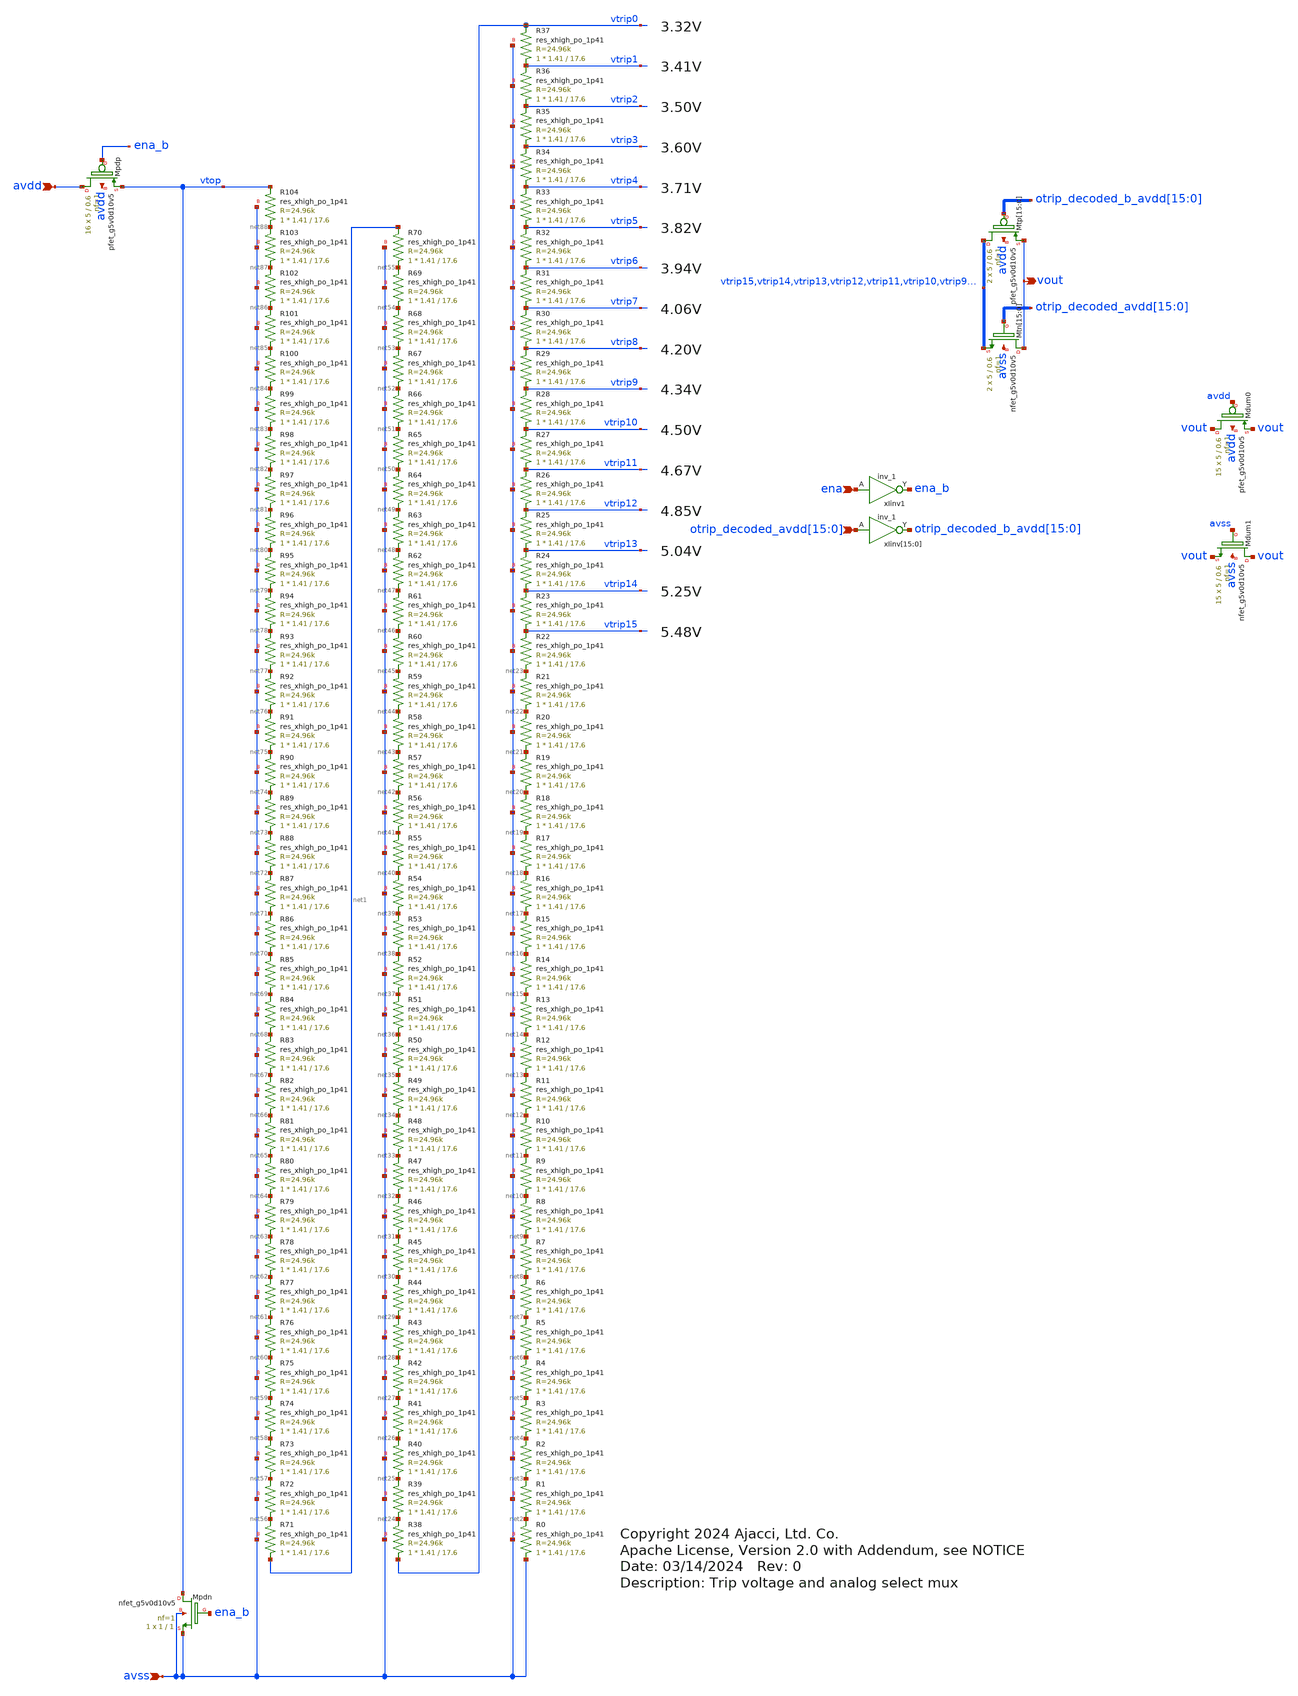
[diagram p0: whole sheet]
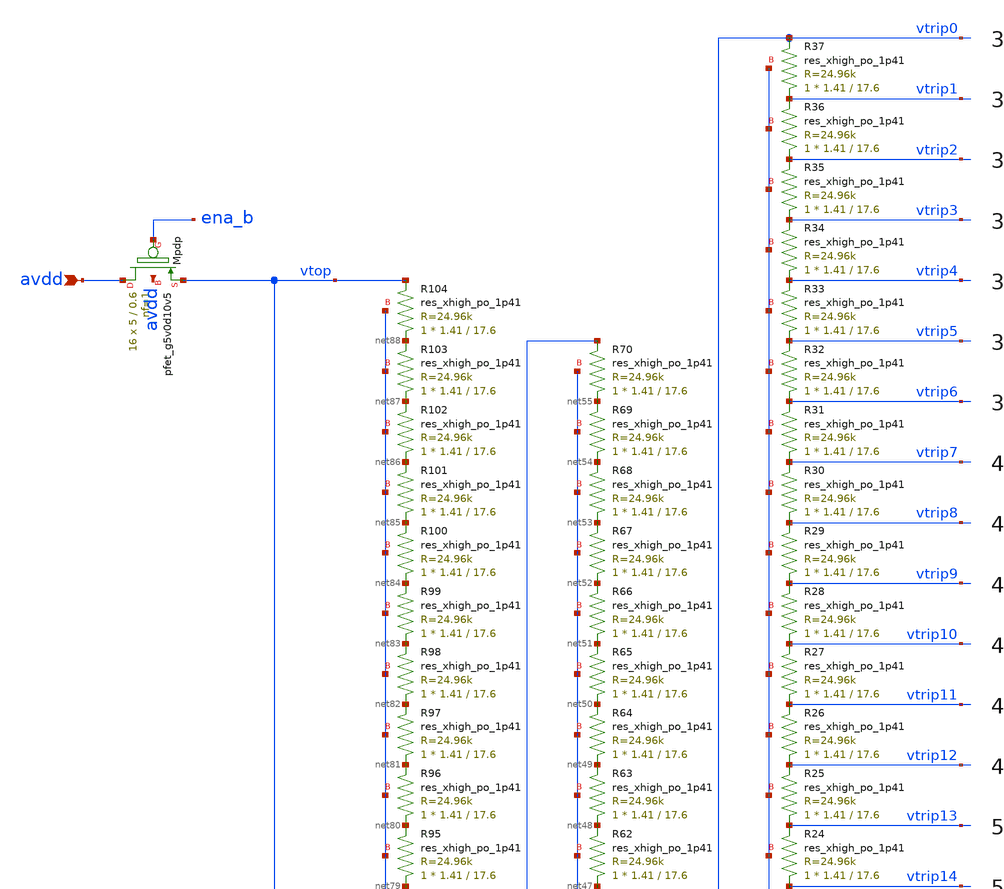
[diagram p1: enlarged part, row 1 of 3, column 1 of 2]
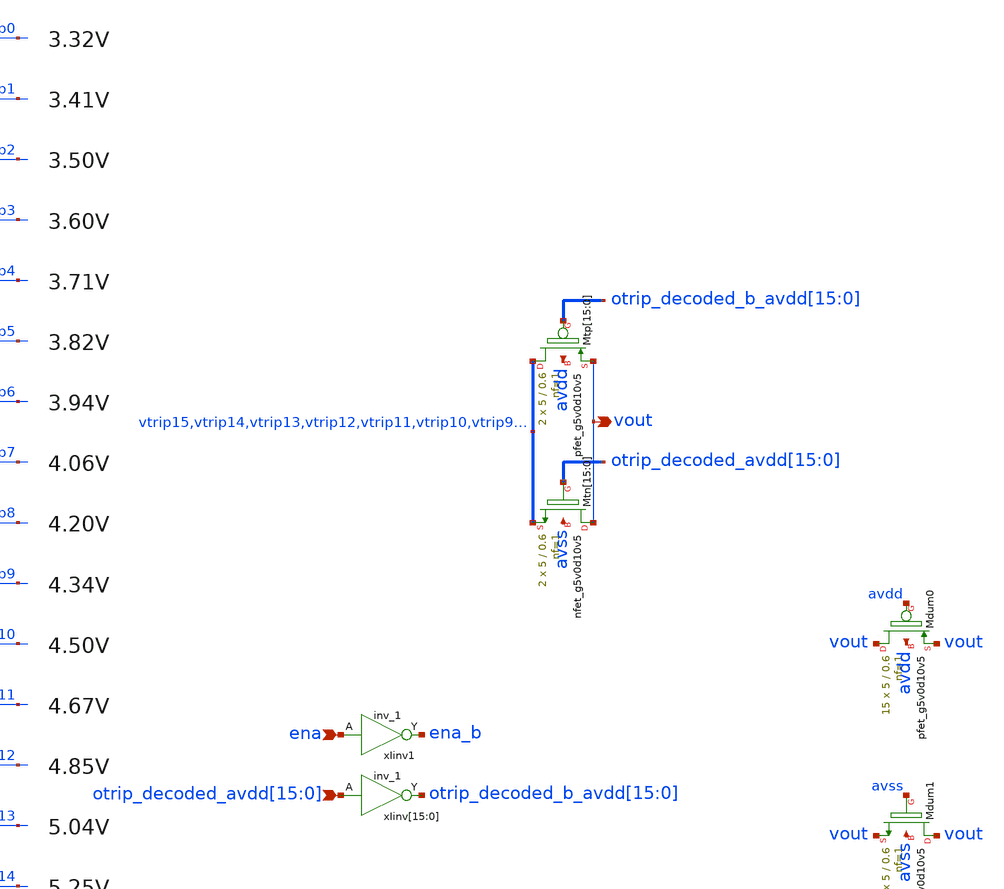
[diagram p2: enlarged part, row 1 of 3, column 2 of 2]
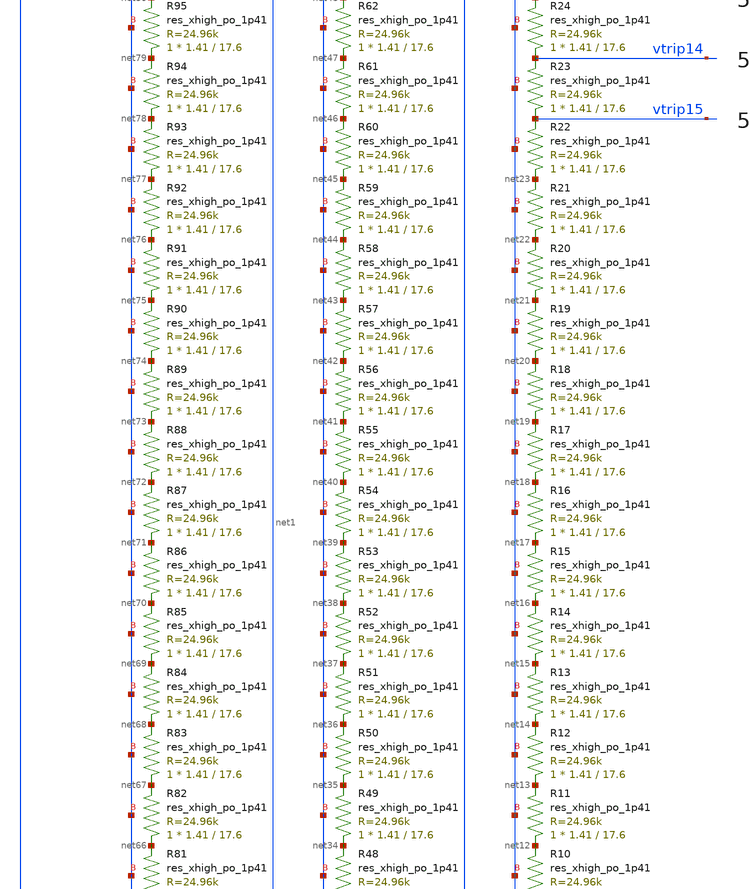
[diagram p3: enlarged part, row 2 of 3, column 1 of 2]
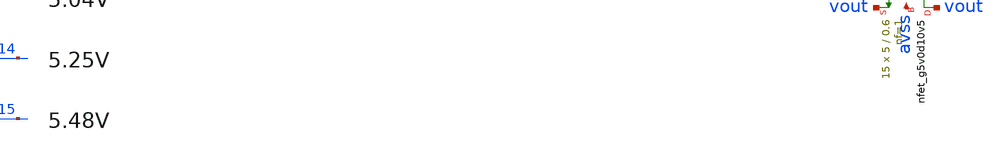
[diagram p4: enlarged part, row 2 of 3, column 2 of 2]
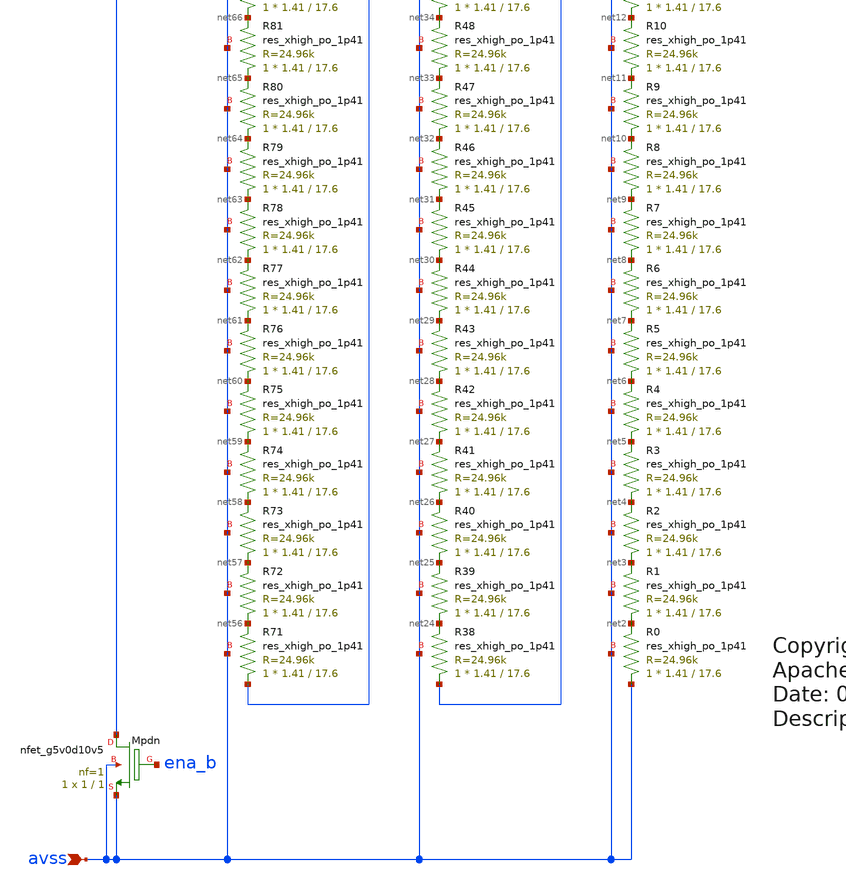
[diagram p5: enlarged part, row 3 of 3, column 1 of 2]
** sch_path: xschem/rstring_mux.sch
* Copyright 2024 Ajacci, Ltd. Co.
* Apache License, Version 2.0 with Addendum, see NOTICE
**.subckt rstring_mux vout
*+ otrip_decoded_avdd[15],otrip_decoded_avdd[14],otrip_decoded_avdd[13],otrip_decoded_avdd[12],otrip_decoded_avdd[11],otrip_decoded_avdd[10],otrip_decoded_avdd[9],otrip_decoded_avdd[8],otrip_decoded_avdd[7],otrip_decoded_avdd[6],otrip_decoded_avdd[5],otrip_decoded_avdd[4],otrip_decoded_avdd[3],otrip_decoded_avdd[2],otrip_decoded_avdd[1],otrip_decoded_avdd[0] avdd avss ena
*.opin vout
*.ipin
*+ otrip_decoded_avdd[15],otrip_decoded_avdd[14],otrip_decoded_avdd[13],otrip_decoded_avdd[12],otrip_decoded_avdd[11],otrip_decoded_avdd[10],otrip_decoded_avdd[9],otrip_decoded_avdd[8],otrip_decoded_avdd[7],otrip_decoded_avdd[6],otrip_decoded_avdd[5],otrip_decoded_avdd[4],otrip_decoded_avdd[3],otrip_decoded_avdd[2],otrip_decoded_avdd[1],otrip_decoded_avdd[0]
*.ipin avdd
*.ipin avss
*.ipin ena
XR1 net2 net3 avss sky130_fd_pr__res_xhigh_po_1p41 L=17.6 mult=1 m=1
XR2 net3 net4 avss sky130_fd_pr__res_xhigh_po_1p41 L=17.6 mult=1 m=1
XR3 net4 net5 avss sky130_fd_pr__res_xhigh_po_1p41 L=17.6 mult=1 m=1
XR4 net5 net6 avss sky130_fd_pr__res_xhigh_po_1p41 L=17.6 mult=1 m=1
XR5 net6 net7 avss sky130_fd_pr__res_xhigh_po_1p41 L=17.6 mult=1 m=1
XR6 net7 net8 avss sky130_fd_pr__res_xhigh_po_1p41 L=17.6 mult=1 m=1
XR7 net8 net9 avss sky130_fd_pr__res_xhigh_po_1p41 L=17.6 mult=1 m=1
XR8 net9 net10 avss sky130_fd_pr__res_xhigh_po_1p41 L=17.6 mult=1 m=1
XR9 net10 net11 avss sky130_fd_pr__res_xhigh_po_1p41 L=17.6 mult=1 m=1
XR10 net11 net12 avss sky130_fd_pr__res_xhigh_po_1p41 L=17.6 mult=1 m=1
XR11 net12 net13 avss sky130_fd_pr__res_xhigh_po_1p41 L=17.6 mult=1 m=1
XR12 net13 net14 avss sky130_fd_pr__res_xhigh_po_1p41 L=17.6 mult=1 m=1
XR13 net14 net15 avss sky130_fd_pr__res_xhigh_po_1p41 L=17.6 mult=1 m=1
XR14 net15 net16 avss sky130_fd_pr__res_xhigh_po_1p41 L=17.6 mult=1 m=1
XR15 net16 net17 avss sky130_fd_pr__res_xhigh_po_1p41 L=17.6 mult=1 m=1
XR16 net17 net18 avss sky130_fd_pr__res_xhigh_po_1p41 L=17.6 mult=1 m=1
XR17 net18 net19 avss sky130_fd_pr__res_xhigh_po_1p41 L=17.6 mult=1 m=1
XR18 net19 net20 avss sky130_fd_pr__res_xhigh_po_1p41 L=17.6 mult=1 m=1
XR19 net20 net21 avss sky130_fd_pr__res_xhigh_po_1p41 L=17.6 mult=1 m=1
XR20 net21 net22 avss sky130_fd_pr__res_xhigh_po_1p41 L=17.6 mult=1 m=1
XR21 net22 net23 avss sky130_fd_pr__res_xhigh_po_1p41 L=17.6 mult=1 m=1
XR22 net23 vtrip15 avss sky130_fd_pr__res_xhigh_po_1p41 L=17.6 mult=1 m=1
XR23 vtrip15 vtrip14 avss sky130_fd_pr__res_xhigh_po_1p41 L=17.6 mult=1 m=1
XR24 vtrip14 vtrip13 avss sky130_fd_pr__res_xhigh_po_1p41 L=17.6 mult=1 m=1
XR25 vtrip13 vtrip12 avss sky130_fd_pr__res_xhigh_po_1p41 L=17.6 mult=1 m=1
XR26 vtrip12 vtrip11 avss sky130_fd_pr__res_xhigh_po_1p41 L=17.6 mult=1 m=1
XR27 vtrip11 vtrip10 avss sky130_fd_pr__res_xhigh_po_1p41 L=17.6 mult=1 m=1
XR28 vtrip10 vtrip9 avss sky130_fd_pr__res_xhigh_po_1p41 L=17.6 mult=1 m=1
XR29 vtrip9 vtrip8 avss sky130_fd_pr__res_xhigh_po_1p41 L=17.6 mult=1 m=1
XR30 vtrip8 vtrip7 avss sky130_fd_pr__res_xhigh_po_1p41 L=17.6 mult=1 m=1
XR31 vtrip7 vtrip6 avss sky130_fd_pr__res_xhigh_po_1p41 L=17.6 mult=1 m=1
XR32 vtrip6 vtrip5 avss sky130_fd_pr__res_xhigh_po_1p41 L=17.6 mult=1 m=1
XR33 vtrip5 vtrip4 avss sky130_fd_pr__res_xhigh_po_1p41 L=17.6 mult=1 m=1
XR34 vtrip4 vtrip3 avss sky130_fd_pr__res_xhigh_po_1p41 L=17.6 mult=1 m=1
XR35 vtrip3 vtrip2 avss sky130_fd_pr__res_xhigh_po_1p41 L=17.6 mult=1 m=1
XR36 vtrip2 vtrip1 avss sky130_fd_pr__res_xhigh_po_1p41 L=17.6 mult=1 m=1
XR37 vtrip1 vtrip0 avss sky130_fd_pr__res_xhigh_po_1p41 L=17.6 mult=1 m=1
XR38 vtrip0 net24 avss sky130_fd_pr__res_xhigh_po_1p41 L=17.6 mult=1 m=1
XR39 net24 net25 avss sky130_fd_pr__res_xhigh_po_1p41 L=17.6 mult=1 m=1
XR40 net25 net26 avss sky130_fd_pr__res_xhigh_po_1p41 L=17.6 mult=1 m=1
XR41 net26 net27 avss sky130_fd_pr__res_xhigh_po_1p41 L=17.6 mult=1 m=1
XR42 net27 net28 avss sky130_fd_pr__res_xhigh_po_1p41 L=17.6 mult=1 m=1
XR43 net28 net29 avss sky130_fd_pr__res_xhigh_po_1p41 L=17.6 mult=1 m=1
XR44 net29 net30 avss sky130_fd_pr__res_xhigh_po_1p41 L=17.6 mult=1 m=1
XR45 net30 net31 avss sky130_fd_pr__res_xhigh_po_1p41 L=17.6 mult=1 m=1
XR46 net31 net32 avss sky130_fd_pr__res_xhigh_po_1p41 L=17.6 mult=1 m=1
XR47 net32 net33 avss sky130_fd_pr__res_xhigh_po_1p41 L=17.6 mult=1 m=1
XR48 net33 net34 avss sky130_fd_pr__res_xhigh_po_1p41 L=17.6 mult=1 m=1
XR49 net34 net35 avss sky130_fd_pr__res_xhigh_po_1p41 L=17.6 mult=1 m=1
XR50 net35 net36 avss sky130_fd_pr__res_xhigh_po_1p41 L=17.6 mult=1 m=1
XR51 net36 net37 avss sky130_fd_pr__res_xhigh_po_1p41 L=17.6 mult=1 m=1
XR52 net37 net38 avss sky130_fd_pr__res_xhigh_po_1p41 L=17.6 mult=1 m=1
XR53 net38 net39 avss sky130_fd_pr__res_xhigh_po_1p41 L=17.6 mult=1 m=1
XR54 net39 net40 avss sky130_fd_pr__res_xhigh_po_1p41 L=17.6 mult=1 m=1
XR55 net40 net41 avss sky130_fd_pr__res_xhigh_po_1p41 L=17.6 mult=1 m=1
XR56 net41 net42 avss sky130_fd_pr__res_xhigh_po_1p41 L=17.6 mult=1 m=1
XR57 net42 net43 avss sky130_fd_pr__res_xhigh_po_1p41 L=17.6 mult=1 m=1
XR58 net43 net44 avss sky130_fd_pr__res_xhigh_po_1p41 L=17.6 mult=1 m=1
XR59 net44 net45 avss sky130_fd_pr__res_xhigh_po_1p41 L=17.6 mult=1 m=1
XR60 net45 net46 avss sky130_fd_pr__res_xhigh_po_1p41 L=17.6 mult=1 m=1
XR61 net46 net47 avss sky130_fd_pr__res_xhigh_po_1p41 L=17.6 mult=1 m=1
XR62 net47 net48 avss sky130_fd_pr__res_xhigh_po_1p41 L=17.6 mult=1 m=1
XR63 net48 net49 avss sky130_fd_pr__res_xhigh_po_1p41 L=17.6 mult=1 m=1
XR64 net49 net50 avss sky130_fd_pr__res_xhigh_po_1p41 L=17.6 mult=1 m=1
XR65 net50 net51 avss sky130_fd_pr__res_xhigh_po_1p41 L=17.6 mult=1 m=1
XR66 net51 net52 avss sky130_fd_pr__res_xhigh_po_1p41 L=17.6 mult=1 m=1
XR67 net52 net53 avss sky130_fd_pr__res_xhigh_po_1p41 L=17.6 mult=1 m=1
XR68 net53 net54 avss sky130_fd_pr__res_xhigh_po_1p41 L=17.6 mult=1 m=1
XR69 net54 net55 avss sky130_fd_pr__res_xhigh_po_1p41 L=17.6 mult=1 m=1
XMtp[15] vtrip15 otrip_decoded_b_avdd[15] vout avdd sky130_fd_pr__pfet_g5v0d10v5 L=0.6 W=5 nf=1 ad='int((nf+1)/2) * W/nf * 0.29'
+ as='int((nf+2)/2) * W/nf * 0.29' pd='2*int((nf+1)/2) * (W/nf + 0.29)' ps='2*int((nf+2)/2) * (W/nf + 0.29)'
+ nrd='0.29 / W' nrs='0.29 / W' sa=0 sb=0 sd=0 mult=2 m=2
XMtp[14] vtrip14 otrip_decoded_b_avdd[14] vout avdd sky130_fd_pr__pfet_g5v0d10v5 L=0.6 W=5 nf=1 ad='int((nf+1)/2) * W/nf * 0.29'
+ as='int((nf+2)/2) * W/nf * 0.29' pd='2*int((nf+1)/2) * (W/nf + 0.29)' ps='2*int((nf+2)/2) * (W/nf + 0.29)'
+ nrd='0.29 / W' nrs='0.29 / W' sa=0 sb=0 sd=0 mult=2 m=2
XMtp[13] vtrip13 otrip_decoded_b_avdd[13] vout avdd sky130_fd_pr__pfet_g5v0d10v5 L=0.6 W=5 nf=1 ad='int((nf+1)/2) * W/nf * 0.29'
+ as='int((nf+2)/2) * W/nf * 0.29' pd='2*int((nf+1)/2) * (W/nf + 0.29)' ps='2*int((nf+2)/2) * (W/nf + 0.29)'
+ nrd='0.29 / W' nrs='0.29 / W' sa=0 sb=0 sd=0 mult=2 m=2
XMtp[12] vtrip12 otrip_decoded_b_avdd[12] vout avdd sky130_fd_pr__pfet_g5v0d10v5 L=0.6 W=5 nf=1 ad='int((nf+1)/2) * W/nf * 0.29'
+ as='int((nf+2)/2) * W/nf * 0.29' pd='2*int((nf+1)/2) * (W/nf + 0.29)' ps='2*int((nf+2)/2) * (W/nf + 0.29)'
+ nrd='0.29 / W' nrs='0.29 / W' sa=0 sb=0 sd=0 mult=2 m=2
XMtp[11] vtrip11 otrip_decoded_b_avdd[11] vout avdd sky130_fd_pr__pfet_g5v0d10v5 L=0.6 W=5 nf=1 ad='int((nf+1)/2) * W/nf * 0.29'
+ as='int((nf+2)/2) * W/nf * 0.29' pd='2*int((nf+1)/2) * (W/nf + 0.29)' ps='2*int((nf+2)/2) * (W/nf + 0.29)'
+ nrd='0.29 / W' nrs='0.29 / W' sa=0 sb=0 sd=0 mult=2 m=2
XMtp[10] vtrip10 otrip_decoded_b_avdd[10] vout avdd sky130_fd_pr__pfet_g5v0d10v5 L=0.6 W=5 nf=1 ad='int((nf+1)/2) * W/nf * 0.29'
+ as='int((nf+2)/2) * W/nf * 0.29' pd='2*int((nf+1)/2) * (W/nf + 0.29)' ps='2*int((nf+2)/2) * (W/nf + 0.29)'
+ nrd='0.29 / W' nrs='0.29 / W' sa=0 sb=0 sd=0 mult=2 m=2
XMtp[9] vtrip9 otrip_decoded_b_avdd[9] vout avdd sky130_fd_pr__pfet_g5v0d10v5 L=0.6 W=5 nf=1 ad='int((nf+1)/2) * W/nf * 0.29'
+ as='int((nf+2)/2) * W/nf * 0.29' pd='2*int((nf+1)/2) * (W/nf + 0.29)' ps='2*int((nf+2)/2) * (W/nf + 0.29)'
+ nrd='0.29 / W' nrs='0.29 / W' sa=0 sb=0 sd=0 mult=2 m=2
XMtp[8] vtrip8 otrip_decoded_b_avdd[8] vout avdd sky130_fd_pr__pfet_g5v0d10v5 L=0.6 W=5 nf=1 ad='int((nf+1)/2) * W/nf * 0.29'
+ as='int((nf+2)/2) * W/nf * 0.29' pd='2*int((nf+1)/2) * (W/nf + 0.29)' ps='2*int((nf+2)/2) * (W/nf + 0.29)'
+ nrd='0.29 / W' nrs='0.29 / W' sa=0 sb=0 sd=0 mult=2 m=2
XMtp[7] vtrip7 otrip_decoded_b_avdd[7] vout avdd sky130_fd_pr__pfet_g5v0d10v5 L=0.6 W=5 nf=1 ad='int((nf+1)/2) * W/nf * 0.29'
+ as='int((nf+2)/2) * W/nf * 0.29' pd='2*int((nf+1)/2) * (W/nf + 0.29)' ps='2*int((nf+2)/2) * (W/nf + 0.29)'
+ nrd='0.29 / W' nrs='0.29 / W' sa=0 sb=0 sd=0 mult=2 m=2
XMtp[6] vtrip6 otrip_decoded_b_avdd[6] vout avdd sky130_fd_pr__pfet_g5v0d10v5 L=0.6 W=5 nf=1 ad='int((nf+1)/2) * W/nf * 0.29'
+ as='int((nf+2)/2) * W/nf * 0.29' pd='2*int((nf+1)/2) * (W/nf + 0.29)' ps='2*int((nf+2)/2) * (W/nf + 0.29)'
+ nrd='0.29 / W' nrs='0.29 / W' sa=0 sb=0 sd=0 mult=2 m=2
XMtp[5] vtrip5 otrip_decoded_b_avdd[5] vout avdd sky130_fd_pr__pfet_g5v0d10v5 L=0.6 W=5 nf=1 ad='int((nf+1)/2) * W/nf * 0.29'
+ as='int((nf+2)/2) * W/nf * 0.29' pd='2*int((nf+1)/2) * (W/nf + 0.29)' ps='2*int((nf+2)/2) * (W/nf + 0.29)'
+ nrd='0.29 / W' nrs='0.29 / W' sa=0 sb=0 sd=0 mult=2 m=2
XMtp[4] vtrip4 otrip_decoded_b_avdd[4] vout avdd sky130_fd_pr__pfet_g5v0d10v5 L=0.6 W=5 nf=1 ad='int((nf+1)/2) * W/nf * 0.29'
+ as='int((nf+2)/2) * W/nf * 0.29' pd='2*int((nf+1)/2) * (W/nf + 0.29)' ps='2*int((nf+2)/2) * (W/nf + 0.29)'
+ nrd='0.29 / W' nrs='0.29 / W' sa=0 sb=0 sd=0 mult=2 m=2
XMtp[3] vtrip3 otrip_decoded_b_avdd[3] vout avdd sky130_fd_pr__pfet_g5v0d10v5 L=0.6 W=5 nf=1 ad='int((nf+1)/2) * W/nf * 0.29'
+ as='int((nf+2)/2) * W/nf * 0.29' pd='2*int((nf+1)/2) * (W/nf + 0.29)' ps='2*int((nf+2)/2) * (W/nf + 0.29)'
+ nrd='0.29 / W' nrs='0.29 / W' sa=0 sb=0 sd=0 mult=2 m=2
XMtp[2] vtrip2 otrip_decoded_b_avdd[2] vout avdd sky130_fd_pr__pfet_g5v0d10v5 L=0.6 W=5 nf=1 ad='int((nf+1)/2) * W/nf * 0.29'
+ as='int((nf+2)/2) * W/nf * 0.29' pd='2*int((nf+1)/2) * (W/nf + 0.29)' ps='2*int((nf+2)/2) * (W/nf + 0.29)'
+ nrd='0.29 / W' nrs='0.29 / W' sa=0 sb=0 sd=0 mult=2 m=2
XMtp[1] vtrip1 otrip_decoded_b_avdd[1] vout avdd sky130_fd_pr__pfet_g5v0d10v5 L=0.6 W=5 nf=1 ad='int((nf+1)/2) * W/nf * 0.29'
+ as='int((nf+2)/2) * W/nf * 0.29' pd='2*int((nf+1)/2) * (W/nf + 0.29)' ps='2*int((nf+2)/2) * (W/nf + 0.29)'
+ nrd='0.29 / W' nrs='0.29 / W' sa=0 sb=0 sd=0 mult=2 m=2
XMtp[0] vtrip0 otrip_decoded_b_avdd[0] vout avdd sky130_fd_pr__pfet_g5v0d10v5 L=0.6 W=5 nf=1 ad='int((nf+1)/2) * W/nf * 0.29'
+ as='int((nf+2)/2) * W/nf * 0.29' pd='2*int((nf+1)/2) * (W/nf + 0.29)' ps='2*int((nf+2)/2) * (W/nf + 0.29)'
+ nrd='0.29 / W' nrs='0.29 / W' sa=0 sb=0 sd=0 mult=2 m=2
XMtn[15] vout otrip_decoded_avdd[15] vtrip15 avss sky130_fd_pr__nfet_g5v0d10v5 L=0.6 W=5 nf=1 ad='int((nf+1)/2) * W/nf * 0.29'
+ as='int((nf+2)/2) * W/nf * 0.29' pd='2*int((nf+1)/2) * (W/nf + 0.29)' ps='2*int((nf+2)/2) * (W/nf + 0.29)'
+ nrd='0.29 / W' nrs='0.29 / W' sa=0 sb=0 sd=0 mult=2 m=2
XMtn[14] vout otrip_decoded_avdd[14] vtrip14 avss sky130_fd_pr__nfet_g5v0d10v5 L=0.6 W=5 nf=1 ad='int((nf+1)/2) * W/nf * 0.29'
+ as='int((nf+2)/2) * W/nf * 0.29' pd='2*int((nf+1)/2) * (W/nf + 0.29)' ps='2*int((nf+2)/2) * (W/nf + 0.29)'
+ nrd='0.29 / W' nrs='0.29 / W' sa=0 sb=0 sd=0 mult=2 m=2
XMtn[13] vout otrip_decoded_avdd[13] vtrip13 avss sky130_fd_pr__nfet_g5v0d10v5 L=0.6 W=5 nf=1 ad='int((nf+1)/2) * W/nf * 0.29'
+ as='int((nf+2)/2) * W/nf * 0.29' pd='2*int((nf+1)/2) * (W/nf + 0.29)' ps='2*int((nf+2)/2) * (W/nf + 0.29)'
+ nrd='0.29 / W' nrs='0.29 / W' sa=0 sb=0 sd=0 mult=2 m=2
XMtn[12] vout otrip_decoded_avdd[12] vtrip12 avss sky130_fd_pr__nfet_g5v0d10v5 L=0.6 W=5 nf=1 ad='int((nf+1)/2) * W/nf * 0.29'
+ as='int((nf+2)/2) * W/nf * 0.29' pd='2*int((nf+1)/2) * (W/nf + 0.29)' ps='2*int((nf+2)/2) * (W/nf + 0.29)'
+ nrd='0.29 / W' nrs='0.29 / W' sa=0 sb=0 sd=0 mult=2 m=2
XMtn[11] vout otrip_decoded_avdd[11] vtrip11 avss sky130_fd_pr__nfet_g5v0d10v5 L=0.6 W=5 nf=1 ad='int((nf+1)/2) * W/nf * 0.29'
+ as='int((nf+2)/2) * W/nf * 0.29' pd='2*int((nf+1)/2) * (W/nf + 0.29)' ps='2*int((nf+2)/2) * (W/nf + 0.29)'
+ nrd='0.29 / W' nrs='0.29 / W' sa=0 sb=0 sd=0 mult=2 m=2
XMtn[10] vout otrip_decoded_avdd[10] vtrip10 avss sky130_fd_pr__nfet_g5v0d10v5 L=0.6 W=5 nf=1 ad='int((nf+1)/2) * W/nf * 0.29'
+ as='int((nf+2)/2) * W/nf * 0.29' pd='2*int((nf+1)/2) * (W/nf + 0.29)' ps='2*int((nf+2)/2) * (W/nf + 0.29)'
+ nrd='0.29 / W' nrs='0.29 / W' sa=0 sb=0 sd=0 mult=2 m=2
XMtn[9] vout otrip_decoded_avdd[9] vtrip9 avss sky130_fd_pr__nfet_g5v0d10v5 L=0.6 W=5 nf=1 ad='int((nf+1)/2) * W/nf * 0.29'
+ as='int((nf+2)/2) * W/nf * 0.29' pd='2*int((nf+1)/2) * (W/nf + 0.29)' ps='2*int((nf+2)/2) * (W/nf + 0.29)'
+ nrd='0.29 / W' nrs='0.29 / W' sa=0 sb=0 sd=0 mult=2 m=2
XMtn[8] vout otrip_decoded_avdd[8] vtrip8 avss sky130_fd_pr__nfet_g5v0d10v5 L=0.6 W=5 nf=1 ad='int((nf+1)/2) * W/nf * 0.29'
+ as='int((nf+2)/2) * W/nf * 0.29' pd='2*int((nf+1)/2) * (W/nf + 0.29)' ps='2*int((nf+2)/2) * (W/nf + 0.29)'
+ nrd='0.29 / W' nrs='0.29 / W' sa=0 sb=0 sd=0 mult=2 m=2
XMtn[7] vout otrip_decoded_avdd[7] vtrip7 avss sky130_fd_pr__nfet_g5v0d10v5 L=0.6 W=5 nf=1 ad='int((nf+1)/2) * W/nf * 0.29'
+ as='int((nf+2)/2) * W/nf * 0.29' pd='2*int((nf+1)/2) * (W/nf + 0.29)' ps='2*int((nf+2)/2) * (W/nf + 0.29)'
+ nrd='0.29 / W' nrs='0.29 / W' sa=0 sb=0 sd=0 mult=2 m=2
XMtn[6] vout otrip_decoded_avdd[6] vtrip6 avss sky130_fd_pr__nfet_g5v0d10v5 L=0.6 W=5 nf=1 ad='int((nf+1)/2) * W/nf * 0.29'
+ as='int((nf+2)/2) * W/nf * 0.29' pd='2*int((nf+1)/2) * (W/nf + 0.29)' ps='2*int((nf+2)/2) * (W/nf + 0.29)'
+ nrd='0.29 / W' nrs='0.29 / W' sa=0 sb=0 sd=0 mult=2 m=2
XMtn[5] vout otrip_decoded_avdd[5] vtrip5 avss sky130_fd_pr__nfet_g5v0d10v5 L=0.6 W=5 nf=1 ad='int((nf+1)/2) * W/nf * 0.29'
+ as='int((nf+2)/2) * W/nf * 0.29' pd='2*int((nf+1)/2) * (W/nf + 0.29)' ps='2*int((nf+2)/2) * (W/nf + 0.29)'
+ nrd='0.29 / W' nrs='0.29 / W' sa=0 sb=0 sd=0 mult=2 m=2
XMtn[4] vout otrip_decoded_avdd[4] vtrip4 avss sky130_fd_pr__nfet_g5v0d10v5 L=0.6 W=5 nf=1 ad='int((nf+1)/2) * W/nf * 0.29'
+ as='int((nf+2)/2) * W/nf * 0.29' pd='2*int((nf+1)/2) * (W/nf + 0.29)' ps='2*int((nf+2)/2) * (W/nf + 0.29)'
+ nrd='0.29 / W' nrs='0.29 / W' sa=0 sb=0 sd=0 mult=2 m=2
XMtn[3] vout otrip_decoded_avdd[3] vtrip3 avss sky130_fd_pr__nfet_g5v0d10v5 L=0.6 W=5 nf=1 ad='int((nf+1)/2) * W/nf * 0.29'
+ as='int((nf+2)/2) * W/nf * 0.29' pd='2*int((nf+1)/2) * (W/nf + 0.29)' ps='2*int((nf+2)/2) * (W/nf + 0.29)'
+ nrd='0.29 / W' nrs='0.29 / W' sa=0 sb=0 sd=0 mult=2 m=2
XMtn[2] vout otrip_decoded_avdd[2] vtrip2 avss sky130_fd_pr__nfet_g5v0d10v5 L=0.6 W=5 nf=1 ad='int((nf+1)/2) * W/nf * 0.29'
+ as='int((nf+2)/2) * W/nf * 0.29' pd='2*int((nf+1)/2) * (W/nf + 0.29)' ps='2*int((nf+2)/2) * (W/nf + 0.29)'
+ nrd='0.29 / W' nrs='0.29 / W' sa=0 sb=0 sd=0 mult=2 m=2
XMtn[1] vout otrip_decoded_avdd[1] vtrip1 avss sky130_fd_pr__nfet_g5v0d10v5 L=0.6 W=5 nf=1 ad='int((nf+1)/2) * W/nf * 0.29'
+ as='int((nf+2)/2) * W/nf * 0.29' pd='2*int((nf+1)/2) * (W/nf + 0.29)' ps='2*int((nf+2)/2) * (W/nf + 0.29)'
+ nrd='0.29 / W' nrs='0.29 / W' sa=0 sb=0 sd=0 mult=2 m=2
XMtn[0] vout otrip_decoded_avdd[0] vtrip0 avss sky130_fd_pr__nfet_g5v0d10v5 L=0.6 W=5 nf=1 ad='int((nf+1)/2) * W/nf * 0.29'
+ as='int((nf+2)/2) * W/nf * 0.29' pd='2*int((nf+1)/2) * (W/nf + 0.29)' ps='2*int((nf+2)/2) * (W/nf + 0.29)'
+ nrd='0.29 / W' nrs='0.29 / W' sa=0 sb=0 sd=0 mult=2 m=2
XR70 net55 net1 avss sky130_fd_pr__res_xhigh_po_1p41 L=17.6 mult=1 m=1
XR71 net1 net56 avss sky130_fd_pr__res_xhigh_po_1p41 L=17.6 mult=1 m=1
XR72 net56 net57 avss sky130_fd_pr__res_xhigh_po_1p41 L=17.6 mult=1 m=1
XR73 net57 net58 avss sky130_fd_pr__res_xhigh_po_1p41 L=17.6 mult=1 m=1
XR74 net58 net59 avss sky130_fd_pr__res_xhigh_po_1p41 L=17.6 mult=1 m=1
XR75 net59 net60 avss sky130_fd_pr__res_xhigh_po_1p41 L=17.6 mult=1 m=1
XR76 net60 net61 avss sky130_fd_pr__res_xhigh_po_1p41 L=17.6 mult=1 m=1
XR77 net61 net62 avss sky130_fd_pr__res_xhigh_po_1p41 L=17.6 mult=1 m=1
XR78 net62 net63 avss sky130_fd_pr__res_xhigh_po_1p41 L=17.6 mult=1 m=1
XR79 net63 net64 avss sky130_fd_pr__res_xhigh_po_1p41 L=17.6 mult=1 m=1
XR80 net64 net65 avss sky130_fd_pr__res_xhigh_po_1p41 L=17.6 mult=1 m=1
XR81 net65 net66 avss sky130_fd_pr__res_xhigh_po_1p41 L=17.6 mult=1 m=1
XR82 net66 net67 avss sky130_fd_pr__res_xhigh_po_1p41 L=17.6 mult=1 m=1
XR83 net67 net68 avss sky130_fd_pr__res_xhigh_po_1p41 L=17.6 mult=1 m=1
XR84 net68 net69 avss sky130_fd_pr__res_xhigh_po_1p41 L=17.6 mult=1 m=1
XR85 net69 net70 avss sky130_fd_pr__res_xhigh_po_1p41 L=17.6 mult=1 m=1
XR86 net70 net71 avss sky130_fd_pr__res_xhigh_po_1p41 L=17.6 mult=1 m=1
XR87 net71 net72 avss sky130_fd_pr__res_xhigh_po_1p41 L=17.6 mult=1 m=1
XR88 net72 net73 avss sky130_fd_pr__res_xhigh_po_1p41 L=17.6 mult=1 m=1
XR89 net73 net74 avss sky130_fd_pr__res_xhigh_po_1p41 L=17.6 mult=1 m=1
XR90 net74 net75 avss sky130_fd_pr__res_xhigh_po_1p41 L=17.6 mult=1 m=1
XR91 net75 net76 avss sky130_fd_pr__res_xhigh_po_1p41 L=17.6 mult=1 m=1
XR92 net76 net77 avss sky130_fd_pr__res_xhigh_po_1p41 L=17.6 mult=1 m=1
XR93 net77 net78 avss sky130_fd_pr__res_xhigh_po_1p41 L=17.6 mult=1 m=1
XR94 net78 net79 avss sky130_fd_pr__res_xhigh_po_1p41 L=17.6 mult=1 m=1
XR95 net79 net80 avss sky130_fd_pr__res_xhigh_po_1p41 L=17.6 mult=1 m=1
XR96 net80 net81 avss sky130_fd_pr__res_xhigh_po_1p41 L=17.6 mult=1 m=1
XR97 net81 net82 avss sky130_fd_pr__res_xhigh_po_1p41 L=17.6 mult=1 m=1
XR98 net82 net83 avss sky130_fd_pr__res_xhigh_po_1p41 L=17.6 mult=1 m=1
XR99 net83 net84 avss sky130_fd_pr__res_xhigh_po_1p41 L=17.6 mult=1 m=1
XR100 net84 net85 avss sky130_fd_pr__res_xhigh_po_1p41 L=17.6 mult=1 m=1
XR101 net85 net86 avss sky130_fd_pr__res_xhigh_po_1p41 L=17.6 mult=1 m=1
XR102 net86 net87 avss sky130_fd_pr__res_xhigh_po_1p41 L=17.6 mult=1 m=1
XR103 net87 net88 avss sky130_fd_pr__res_xhigh_po_1p41 L=17.6 mult=1 m=1
xIinv[15] otrip_decoded_avdd[15] avss avss avdd avdd otrip_decoded_b_avdd[15]
+ sky130_fd_sc_hvl__inv_1
xIinv[14] otrip_decoded_avdd[14] avss avss avdd avdd otrip_decoded_b_avdd[14]
+ sky130_fd_sc_hvl__inv_1
xIinv[13] otrip_decoded_avdd[13] avss avss avdd avdd otrip_decoded_b_avdd[13]
+ sky130_fd_sc_hvl__inv_1
xIinv[12] otrip_decoded_avdd[12] avss avss avdd avdd otrip_decoded_b_avdd[12]
+ sky130_fd_sc_hvl__inv_1
xIinv[11] otrip_decoded_avdd[11] avss avss avdd avdd otrip_decoded_b_avdd[11]
+ sky130_fd_sc_hvl__inv_1
xIinv[10] otrip_decoded_avdd[10] avss avss avdd avdd otrip_decoded_b_avdd[10]
+ sky130_fd_sc_hvl__inv_1
xIinv[9] otrip_decoded_avdd[9] avss avss avdd avdd otrip_decoded_b_avdd[9] sky130_fd_sc_hvl__inv_1
xIinv[8] otrip_decoded_avdd[8] avss avss avdd avdd otrip_decoded_b_avdd[8] sky130_fd_sc_hvl__inv_1
xIinv[7] otrip_decoded_avdd[7] avss avss avdd avdd otrip_decoded_b_avdd[7] sky130_fd_sc_hvl__inv_1
xIinv[6] otrip_decoded_avdd[6] avss avss avdd avdd otrip_decoded_b_avdd[6] sky130_fd_sc_hvl__inv_1
xIinv[5] otrip_decoded_avdd[5] avss avss avdd avdd otrip_decoded_b_avdd[5] sky130_fd_sc_hvl__inv_1
xIinv[4] otrip_decoded_avdd[4] avss avss avdd avdd otrip_decoded_b_avdd[4] sky130_fd_sc_hvl__inv_1
xIinv[3] otrip_decoded_avdd[3] avss avss avdd avdd otrip_decoded_b_avdd[3] sky130_fd_sc_hvl__inv_1
xIinv[2] otrip_decoded_avdd[2] avss avss avdd avdd otrip_decoded_b_avdd[2] sky130_fd_sc_hvl__inv_1
xIinv[1] otrip_decoded_avdd[1] avss avss avdd avdd otrip_decoded_b_avdd[1] sky130_fd_sc_hvl__inv_1
xIinv[0] otrip_decoded_avdd[0] avss avss avdd avdd otrip_decoded_b_avdd[0] sky130_fd_sc_hvl__inv_1
XR0 avss net2 avss sky130_fd_pr__res_xhigh_po_1p41 L=17.6 mult=1 m=1
XR104 net88 vtop avss sky130_fd_pr__res_xhigh_po_1p41 L=17.6 mult=1 m=1
XMpdn vtop ena_b avss avss sky130_fd_pr__nfet_g5v0d10v5 L=1 W=1 nf=1 ad='int((nf+1)/2) * W/nf * 0.29'
+ as='int((nf+2)/2) * W/nf * 0.29' pd='2*int((nf+1)/2) * (W/nf + 0.29)' ps='2*int((nf+2)/2) * (W/nf + 0.29)'
+ nrd='0.29 / W' nrs='0.29 / W' sa=0 sb=0 sd=0 mult=1 m=1
XMpdp avdd ena_b vtop avdd sky130_fd_pr__pfet_g5v0d10v5 L=0.6 W=5 nf=1 ad='int((nf+1)/2) * W/nf * 0.29'
+ as='int((nf+2)/2) * W/nf * 0.29' pd='2*int((nf+1)/2) * (W/nf + 0.29)' ps='2*int((nf+2)/2) * (W/nf + 0.29)'
+ nrd='0.29 / W' nrs='0.29 / W' sa=0 sb=0 sd=0 mult=16 m=16
xIinv1 ena avss avss avdd avdd ena_b sky130_fd_sc_hvl__inv_1
XMdum0 vout avdd vout avdd sky130_fd_pr__pfet_g5v0d10v5 L=0.6 W=5 nf=1 ad='int((nf+1)/2) * W/nf * 0.29'
+ as='int((nf+2)/2) * W/nf * 0.29' pd='2*int((nf+1)/2) * (W/nf + 0.29)' ps='2*int((nf+2)/2) * (W/nf + 0.29)'
+ nrd='0.29 / W' nrs='0.29 / W' sa=0 sb=0 sd=0 mult=15 m=15
XMdum1 vout avss vout avss sky130_fd_pr__nfet_g5v0d10v5 L=0.6 W=5 nf=1 ad='int((nf+1)/2) * W/nf * 0.29'
+ as='int((nf+2)/2) * W/nf * 0.29' pd='2*int((nf+1)/2) * (W/nf + 0.29)' ps='2*int((nf+2)/2) * (W/nf + 0.29)'
+ nrd='0.29 / W' nrs='0.29 / W' sa=0 sb=0 sd=0 mult=15 m=15
**.ends
.end
